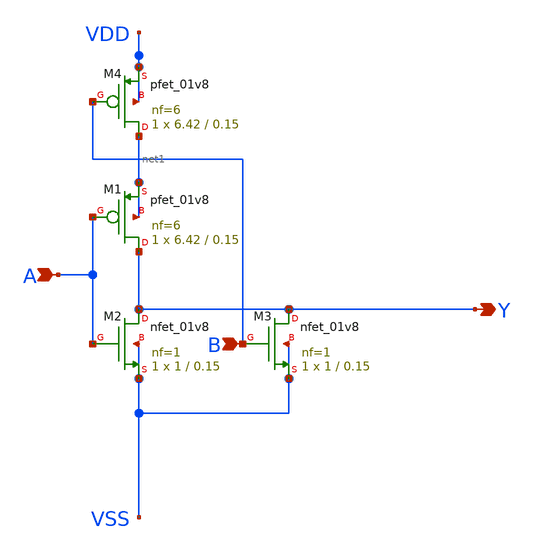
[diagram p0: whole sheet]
** sch_path: design/xschem/NOR/nor2.sch
**.subckt nor2 A Y B
*.ipin A
*.opin Y
*.ipin B
XM1 Y A net1 net1 sky130_fd_pr__pfet_01v8 L=0.15 W=6.42 nf=6 ad='int((nf+1)/2) * W/nf * 0.29' as='int((nf+2)/2) * W/nf * 0.29'
+ pd='2*int((nf+1)/2) * (W/nf + 0.29)' ps='2*int((nf+2)/2) * (W/nf + 0.29)' nrd='0.29 / W' nrs='0.29 / W'
+ sa=0 sb=0 sd=0 mult=1 m=1
XM2 Y A VSS VSS sky130_fd_pr__nfet_01v8 L=0.15 W=1 nf=1 ad='int((nf+1)/2) * W/nf * 0.29' as='int((nf+2)/2) * W/nf * 0.29'
+ pd='2*int((nf+1)/2) * (W/nf + 0.29)' ps='2*int((nf+2)/2) * (W/nf + 0.29)' nrd='0.29 / W' nrs='0.29 / W'
+ sa=0 sb=0 sd=0 mult=1 m=1
XM3 Y B VSS VSS sky130_fd_pr__nfet_01v8 L=0.15 W=1 nf=1 ad='int((nf+1)/2) * W/nf * 0.29' as='int((nf+2)/2) * W/nf * 0.29'
+ pd='2*int((nf+1)/2) * (W/nf + 0.29)' ps='2*int((nf+2)/2) * (W/nf + 0.29)' nrd='0.29 / W' nrs='0.29 / W'
+ sa=0 sb=0 sd=0 mult=1 m=1
XM4 net1 B VDD VDD sky130_fd_pr__pfet_01v8 L=0.15 W=6.42 nf=6 ad='int((nf+1)/2) * W/nf * 0.29' as='int((nf+2)/2) * W/nf * 0.29'
+ pd='2*int((nf+1)/2) * (W/nf + 0.29)' ps='2*int((nf+2)/2) * (W/nf + 0.29)' nrd='0.29 / W' nrs='0.29 / W'
+ sa=0 sb=0 sd=0 mult=1 m=1
**.ends
.end
